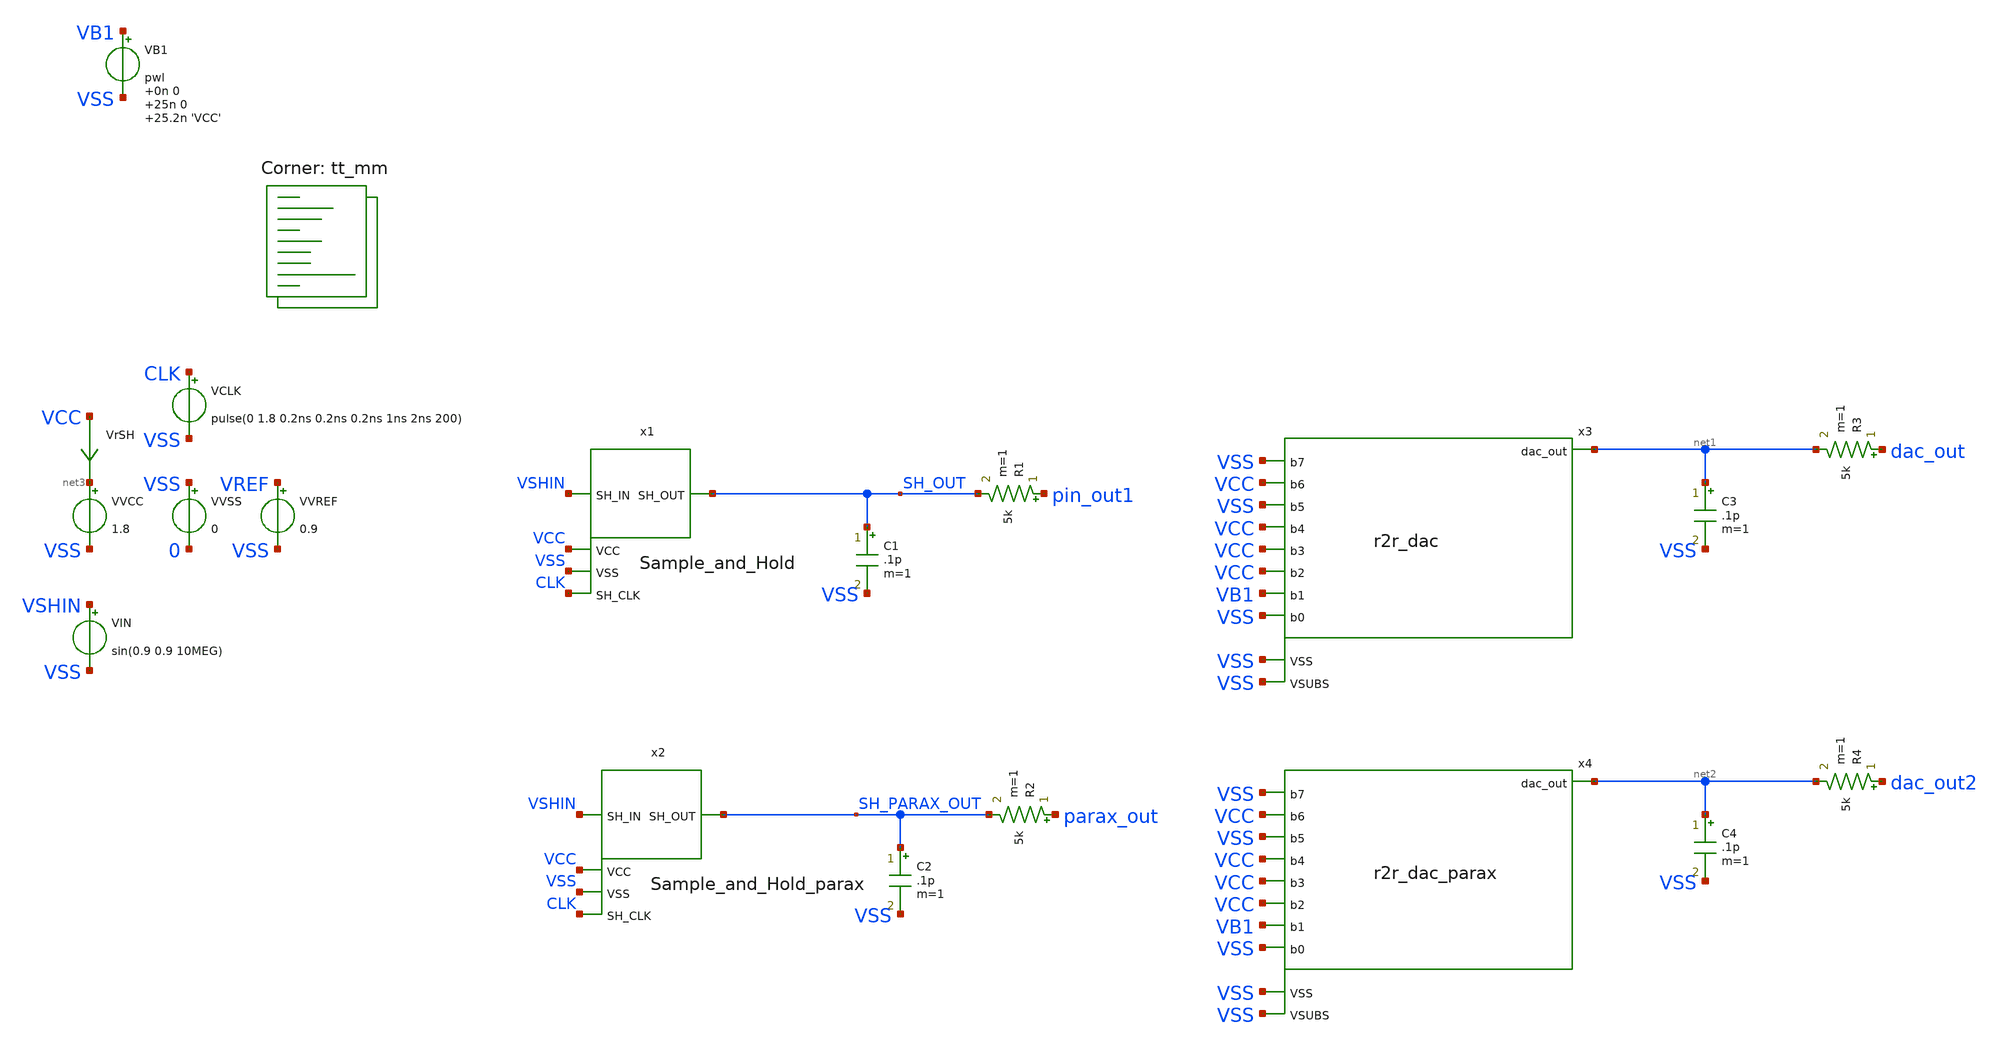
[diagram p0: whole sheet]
** sch_path: xschem/testbench.sch
**.subckt testbench
x1 SH_OUT VSHIN VSS VCC CLK Sample_and_Hold
VCLK CLK VSS pulse(0 1.8 0.2ns 0.2ns 0.2ns 1ns 2ns 200)
VVCC net3 VSS 1.8
VVSS VSS 0 0
VIN VSHIN VSS sin(0.9 0.9 10MEG)
VVREF VREF VSS 0.9
R1 pin_out1 SH_OUT 5k m=1
C1 SH_OUT VSS .1p m=1
VrSH VCC net3 0
.save i(vrsh)
x2 SH_PARAX_OUT VSHIN VSS VCC CLK Sample_and_Hold_parax
R2 parax_out SH_PARAX_OUT 5k m=1
C2 SH_PARAX_OUT VSS .1p m=1
x3 net1 VSS VB1 VCC VCC VSS VSS VCC VCC VSS VSS r2r_dac
VB1 VB1 VSS pwl 0n 0 25n 0 25.2n 'VCC'
R3 dac_out net1 5k m=1
C3 net1 VSS .1p m=1
x4 net2 VSS VB1 VCC VCC VSS VSS VCC VCC VSS VSS r2r_dac_parax
R4 dac_out2 net2 5k m=1
C4 net2 VSS .1p m=1
**** begin user architecture code
.lib $::SKYWATER_MODELS/sky130.lib.spice tt_mm


.option chgtol=4e-16 method=gear
.param VCC = 1.8
.param VREF = 0.9
.param temp = 25
*vvcc VCC 0 1.8
*vvss VSS 0 0
*vvref VREF 0 0.9
*vclk CLK pulse(1ns 1ns 1ns 5ns 10ns 25)
*vvshin VSHIN sin(0.9 0.9 10MEG)


.control
  save all
  savecurrents
  op
  write testbench.raw
  reset
  set appendwrite
  *repeat 5
    save all
    tran 0.1n 250n uic
    write testbench.raw
    set appendwrite
    reset
  *end
  quit 0
.endc

**** end user architecture code
**.ends
.end
